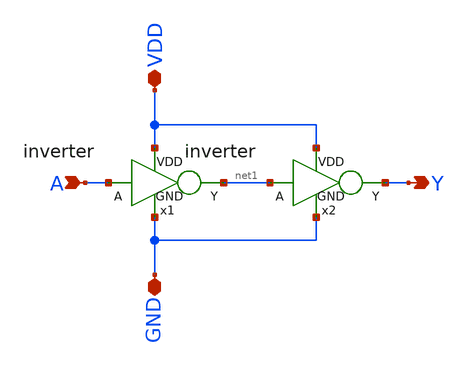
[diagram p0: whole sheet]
** sch_path: designs/buffer/xschem/buffer.sch
**.subckt buffer A Y VDD GND
*.ipin A
*.opin Y
*.iopin VDD
*.iopin GND
x1 VDD A net1 GND inverter
x2 VDD net1 Y GND inverter
**.ends

* expanding   symbol:  inverter.sym # of pins=4
** sym_path: designs/inverter/xschem/inverter.sym
** sch_path: designs/inverter/xschem/inverter.sch
.subckt inverter VDD A Y GND
input p1
output p2
inout p3
inout p4
XM1 net1 net2 net4 net4 sky130_fd_pr__nfet_01v8 L=0.15 W=1 nf=1 ad='int((1 + 1)/2) * 1 / 1 * 0.29' as='int((1 + 2)/2) * 1 / 1 * 0.29'
+ pd='2*int((1 + 1)/2) * (1 / 1 + 0.29)' ps='2*int((1 + 2)/2) * (1 / 1 + 0.29)' nrd='0.29 / 1 ' nrs='0.29 / 1 '
+ sa=0 sb=0 sd=0 mult=1 m=1
XM2 net1 net2 net3 net3 sky130_fd_pr__pfet_01v8 L=0.15 W=1 nf=1 ad='int((1 + 1)/2) * 1 / 1 * 0.29' as='int((1 + 2)/2) * 1 / 1 * 0.29'
+ pd='2*int((1 + 1)/2) * (1 / 1 + 0.29)' ps='2*int((1 + 2)/2) * (1 / 1 + 0.29)' nrd='0.29 / 1 ' nrs='0.29 / 1 '
+ sa=0 sb=0 sd=0 mult=1 m=1
.ends

.end
